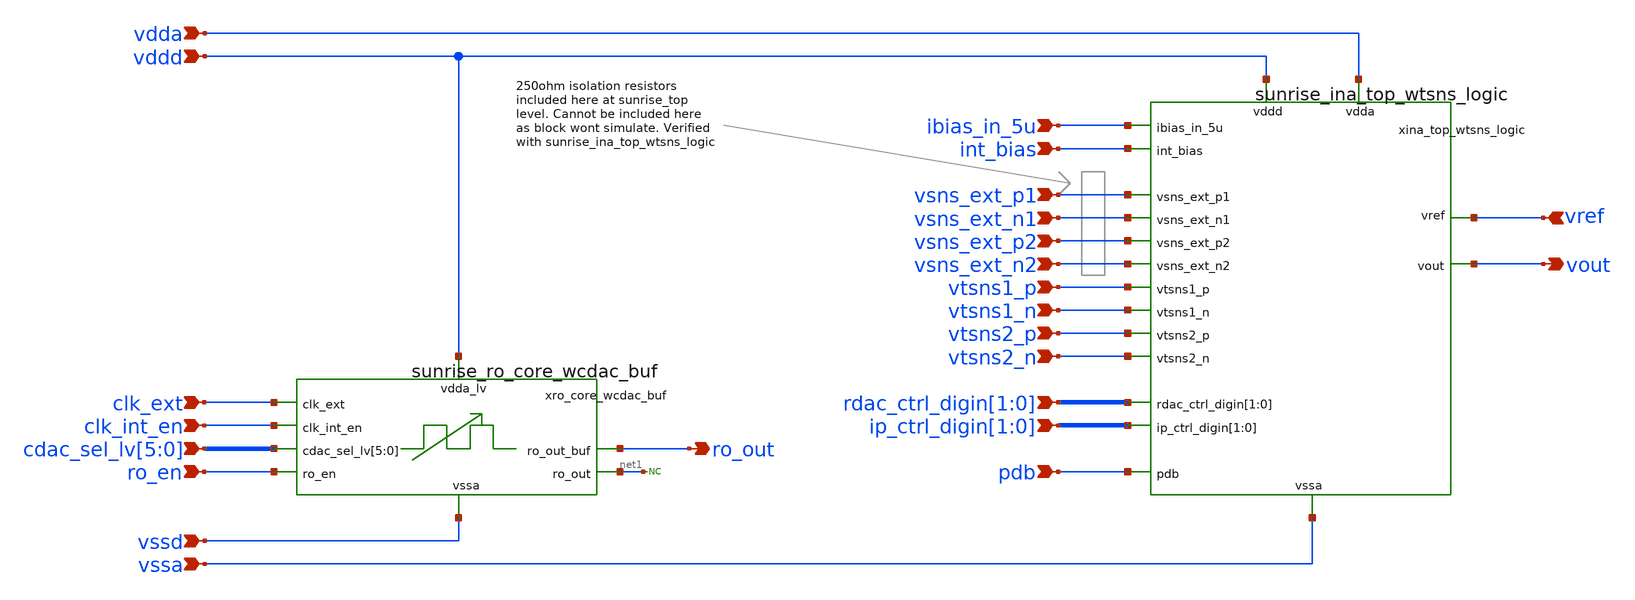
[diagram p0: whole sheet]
** sch_path: Schematics_Layout/sunrise_ana_top/sunrise_ana_top.sch
**.subckt sunrise_ana_top ibias_in_5u vtsns1_p vtsns1_n vtsns2_p vtsns2_n int_bias
*+ ip_ctrl_digin[1],ip_ctrl_digin[0] rdac_ctrl_digin[1],rdac_ctrl_digin[0] pdb clk_ext clk_int_en
*+ cdac_sel_lv[5],cdac_sel_lv[4],cdac_sel_lv[3],cdac_sel_lv[2],cdac_sel_lv[1],cdac_sel_lv[0] ro_en vref vout ro_out vdda vddd vssa vssd vsns_ext_p1 vsns_ext_n1 vsns_ext_p2 vsns_ext_n2
*.ipin ibias_in_5u
*.ipin vtsns1_p
*.ipin vtsns1_n
*.ipin vtsns2_p
*.ipin vtsns2_n
*.ipin int_bias
*.ipin ip_ctrl_digin[1],ip_ctrl_digin[0]
*.ipin rdac_ctrl_digin[1],rdac_ctrl_digin[0]
*.ipin pdb
*.ipin clk_ext
*.ipin clk_int_en
*.ipin cdac_sel_lv[5],cdac_sel_lv[4],cdac_sel_lv[3],cdac_sel_lv[2],cdac_sel_lv[1],cdac_sel_lv[0]
*.ipin ro_en
*.ipin vref
*.opin vout
*.opin ro_out
*.ipin vdda
*.ipin vddd
*.ipin vssa
*.ipin vssd
*.ipin vsns_ext_p1
*.ipin vsns_ext_n1
*.ipin vsns_ext_p2
*.ipin vsns_ext_n2
xina_top_wtsns_logic vdda vddd ibias_in_5u vsns_ext_p1 vsns_ext_n1 int_bias vref vtsns1_p
+ ip_ctrl_digin[1] ip_ctrl_digin[0] vtsns1_n rdac_ctrl_digin[1] rdac_ctrl_digin[0] vout pdb vsns_ext_p2 vsns_ext_n2
+ vtsns2_p vtsns2_n vssa sunrise_ina_top_wtsns_logic
xro_core_wcdac_buf vddd ro_out cdac_sel_lv[5] cdac_sel_lv[4] cdac_sel_lv[3] cdac_sel_lv[2]
+ cdac_sel_lv[1] cdac_sel_lv[0] ro_en vssd net1 clk_ext clk_int_en sunrise_ro_core_wcdac_buf
* noconn #net1
**.ends
.end
